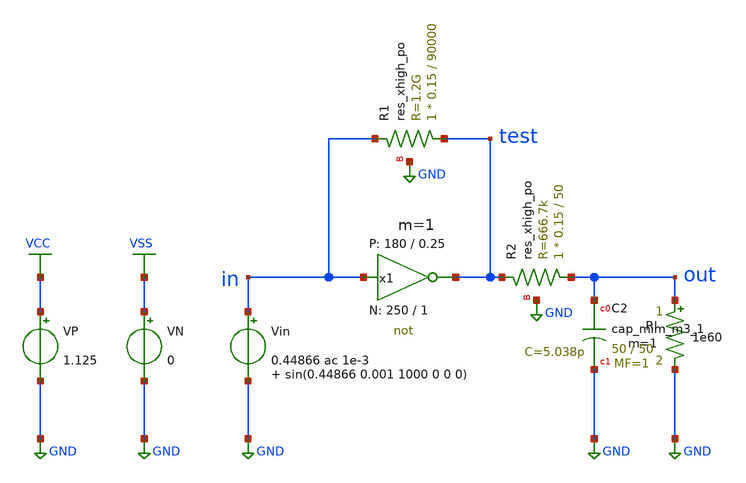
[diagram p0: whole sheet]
** sch_path: Amplifier_Inv/xschem/DC_tb_v1.sch
* StefanSchippers/xschem_sky130/sky130_tests/not.sch:
* Copyright 2021 Stefan Frederik Schippers
* Licensed under the Apache License, Version 2.0 (the "License");
**.subckt DC_tb_v1
VN VSS GND 0
VP VCC GND 1.125
.save i(vp)
Vin in GND 0.44866 ac 1e-3 sin(0.44866 0.001 1000 0 0 0)
.save i(vin)
Rl out GND 1e60 m=1
x1 test in VCC VSS not W_N=250 L_N=1 W_P=180 L_P=0.25 m=1
XC2 out GND sky130_fd_pr__cap_mim_m3_1 W=50 L=50 MF=1 m=1
XR1 test in GND sky130_fd_pr__res_xhigh_po W=0.15 L=90000 mult=1 m=1
XR2 out test GND sky130_fd_pr__res_xhigh_po W=0.15 L=50 mult=1 m=1
**** begin user architecture code

** opencircuitdesign pdks install
.lib $::SKYWATER_MODELS/sky130.lib.spice tt



.control

  dc Vin 0 1 0.00001
  save all v(in) v(out)
  write tb_inv_sky130_a_DC_v1.raw v(in) v(out)

.endc


**** end user architecture code
**.ends

* expanding   symbol:  sky130_tests/not.sym # of pins=2
** sym_path: sky130_tests/not.sym
** sch_path: sky130_tests/not.sch
.subckt not y a VCCPIN VSSPIN     W_N=1 L_N=0.15 W_P=2 L_P=0.15
*.opin y
*.ipin a
XM1 DN a VSSPIN VSSPIN sky130_fd_pr__nfet_01v8 L=L_N W=W_N nf=1 ad='int((1 + 1)/2) * W_N / 1 * 0.29'
+ as='int((1 + 2)/2) * W_N / 1 * 0.29' pd='2*int((1 + 1)/2) * (W_N / 1 + 0.29)' ps='2*int((1 + 2)/2) * (W_N / 1 + 0.29)'
+ nrd='0.29 / W_N ' nrs='0.29 / W_N ' sa=0 sb=0 sd=0 mult=1 m=1
XM2 DP a VCCPIN VCCPIN sky130_fd_pr__pfet_01v8 L=L_P W=W_P nf=1 ad='int((nf+1)/2) * W/nf * 0.29' as='int((nf+2)/2) * W/nf * 0.29'
+ pd='2*int((nf+1)/2) * (W/nf + 0.29)' ps='2*int((nf+2)/2) * (W/nf + 0.29)' nrd='0.29 / W' nrs='0.29 / W'
+ sa=0 sb=0 sd=0 mult=1 m=1
Vmeas DP y 0
.save i(vmeas)
Vmeas1 y DN 0
.save i(vmeas1)
.save v(dp)
.save v(dn)
.ends

.GLOBAL GND
.GLOBAL VSS
.GLOBAL VCC
.end
